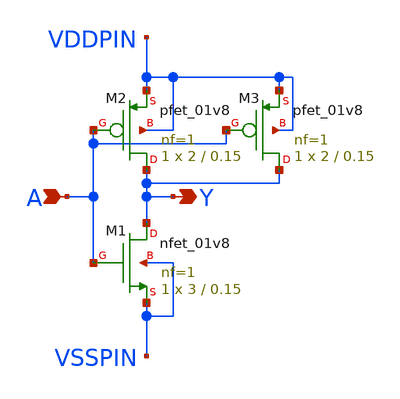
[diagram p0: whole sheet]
** sch_path: sky130A/libs.tech/xschem/sky130_tests/INVX1.sch
**.subckt INVX1 A Y
*.ipin A
*.opin Y
XM1 Y A VSSPIN VSSPIN sky130_fd_pr__nfet_01v8 L=0.15 W=3 nf=1 ad='int((nf+1)/2) * W/nf * 0.29' as='int((nf+2)/2) * W/nf * 0.29'
+ pd='2*int((nf+1)/2) * (W/nf + 0.29)' ps='2*int((nf+2)/2) * (W/nf + 0.29)' nrd='0.29 / W' nrs='0.29 / W'
+ sa=0 sb=0 sd=0 mult=1 m=1
XM2 Y A VDDPIN VDDPIN sky130_fd_pr__pfet_01v8 L=0.15 W=2 nf=1 ad='int((nf+1)/2) * W/nf * 0.29' as='int((nf+2)/2) * W/nf * 0.29'
+ pd='2*int((nf+1)/2) * (W/nf + 0.29)' ps='2*int((nf+2)/2) * (W/nf + 0.29)' nrd='0.29 / W' nrs='0.29 / W'
+ sa=0 sb=0 sd=0 mult=1 m=1
XM3 Y A VDDPIN VDDPIN sky130_fd_pr__pfet_01v8 L=0.15 W=2 nf=1 ad='int((nf+1)/2) * W/nf * 0.29' as='int((nf+2)/2) * W/nf * 0.29'
+ pd='2*int((nf+1)/2) * (W/nf + 0.29)' ps='2*int((nf+2)/2) * (W/nf + 0.29)' nrd='0.29 / W' nrs='0.29 / W'
+ sa=0 sb=0 sd=0 mult=1 m=1
**.ends
.end
